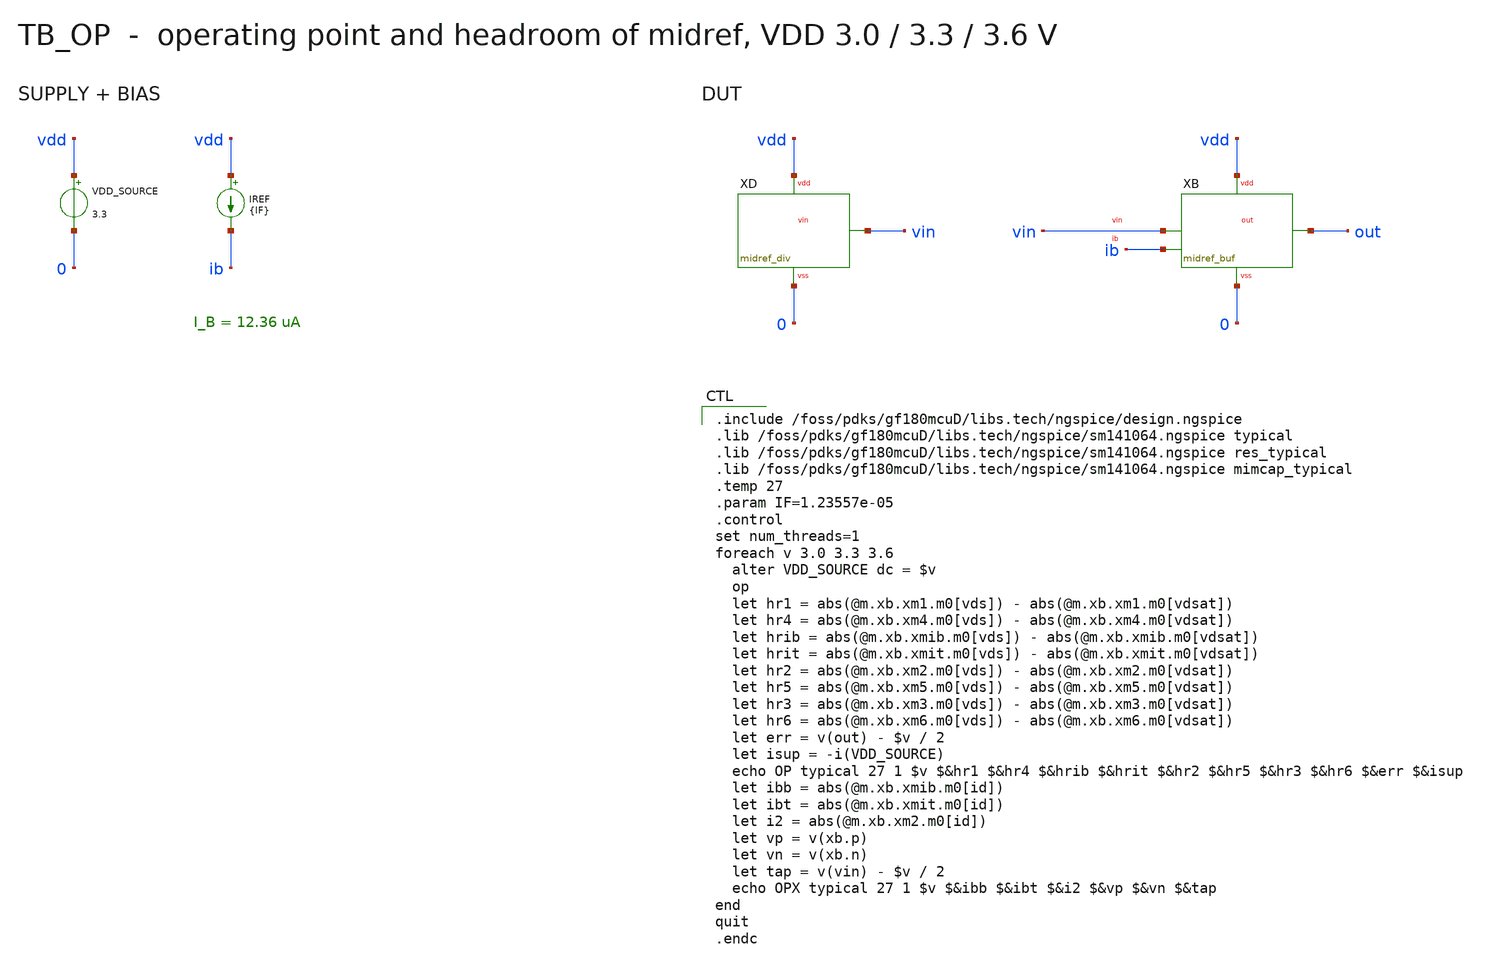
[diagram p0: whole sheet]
** sch_path: mixed_signal/midrail_ref/tb_op.sch
**.subckt tb_op
VDD_SOURCE vdd 0 3.3
IREF vdd ib {IF}
XD vin vdd 0 midref_div
XB out vin ib vdd 0 midref_buf
**** begin user architecture code

.include /foss/pdks/gf180mcuD/libs.tech/ngspice/design.ngspice
.lib /foss/pdks/gf180mcuD/libs.tech/ngspice/sm141064.ngspice typical
.lib /foss/pdks/gf180mcuD/libs.tech/ngspice/sm141064.ngspice res_typical
.lib /foss/pdks/gf180mcuD/libs.tech/ngspice/sm141064.ngspice mimcap_typical
.temp 27
.param IF=1.23557e-05
.control
set num_threads=1
foreach v 3.0 3.3 3.6
  alter VDD_SOURCE dc = $v
  op
  let hr1 = abs(@m.xb.xm1.m0[vds]) - abs(@m.xb.xm1.m0[vdsat])
  let hr4 = abs(@m.xb.xm4.m0[vds]) - abs(@m.xb.xm4.m0[vdsat])
  let hrib = abs(@m.xb.xmib.m0[vds]) - abs(@m.xb.xmib.m0[vdsat])
  let hrit = abs(@m.xb.xmit.m0[vds]) - abs(@m.xb.xmit.m0[vdsat])
  let hr2 = abs(@m.xb.xm2.m0[vds]) - abs(@m.xb.xm2.m0[vdsat])
  let hr5 = abs(@m.xb.xm5.m0[vds]) - abs(@m.xb.xm5.m0[vdsat])
  let hr3 = abs(@m.xb.xm3.m0[vds]) - abs(@m.xb.xm3.m0[vdsat])
  let hr6 = abs(@m.xb.xm6.m0[vds]) - abs(@m.xb.xm6.m0[vdsat])
  let err = v(out) - $v / 2
  let isup = -i(VDD_SOURCE)
  echo OP typical 27 1 $v $&hr1 $&hr4 $&hrib $&hrit $&hr2 $&hr5 $&hr3 $&hr6 $&err $&isup
  let ibb = abs(@m.xb.xmib.m0[id])
  let ibt = abs(@m.xb.xmit.m0[id])
  let i2 = abs(@m.xb.xm2.m0[id])
  let vp = v(xb.p)
  let vn = v(xb.n)
  let tap = v(vin) - $v / 2
  echo OPX typical 27 1 $v $&ibb $&ibt $&i2 $&vp $&vn $&tap
end
quit
.endc

**** end user architecture code
**.ends
.end
